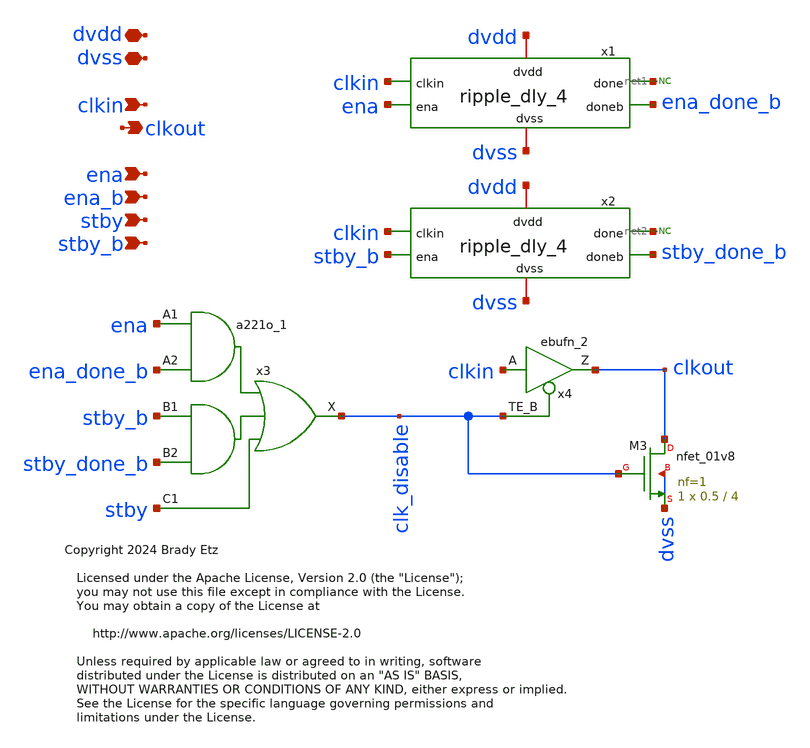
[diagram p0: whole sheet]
** sch_path: xschem/ripl_dly_clk_buf.sch
* Copyright 2024 Brady Etz
* Licensed under the Apache License, Version 2.0 (the "License");
**.subckt ripl_dly_clk_buf dvdd dvss clkin clkout ena stby ena_b stby_b
*.iopin dvdd
*.iopin dvss
*.ipin clkin
*.opin clkout
*.ipin ena
*.ipin stby
*.ipin ena_b
*.ipin stby_b
XM3 clkout clk_disable dvss dvss sky130_fd_pr__nfet_01v8 L=4 W=0.5 nf=1 ad='int((nf+1)/2) * W/nf * 0.29'
+ as='int((nf+2)/2) * W/nf * 0.29' pd='2*int((nf+1)/2) * (W/nf + 0.29)' ps='2*int((nf+2)/2) * (W/nf + 0.29)'
+ nrd='0.29 / W' nrs='0.29 / W' sa=0 sb=0 sd=0 mult=1 m=1
x4 clkin clk_disable dvss dvss dvdd dvdd clkout sky130_fd_sc_hd__ebufn_2
* noconn #net1
* noconn #net2
x3 ena ena_done_b stby_b stby_done_b stby dvss dvss dvdd dvdd clk_disable sky130_fd_sc_hd__a221o_1
x2 dvdd dvss clkin net2 stby_done_b stby_b ripple_dly_4
x1 dvdd dvss clkin net1 ena_done_b ena ripple_dly_4
**.ends

* expanding   symbol:  ripple_dly_4.sym # of pins=6
** sym_path: xschem/ripple_dly_4.sym
** sch_path: xschem/ripple_dly_4.sch
.subckt ripple_dly_4 dvdd dvss clkin done doneb ena
*.ipin clkin
*.ipin ena
*.opin done
*.opin doneb
*.iopin dvdd
*.iopin dvss
x2 gated_clk Qb1 ena dvss dvss dvdd dvdd net1 Qb1 sky130_fd_sc_hd__dfrbp_1
x3 Qb1 Qb2 ena dvss dvss dvdd dvdd net2 Qb2 sky130_fd_sc_hd__dfrbp_1
x1 clkin doneb dvss dvss dvdd dvdd gated_clk sky130_fd_sc_hd__nand2_1
* noconn #net1
* noconn #net2
x4 Qb2 doneb ena dvss dvss dvdd dvdd done doneb sky130_fd_sc_hd__dfrbp_1
.ends

.end
